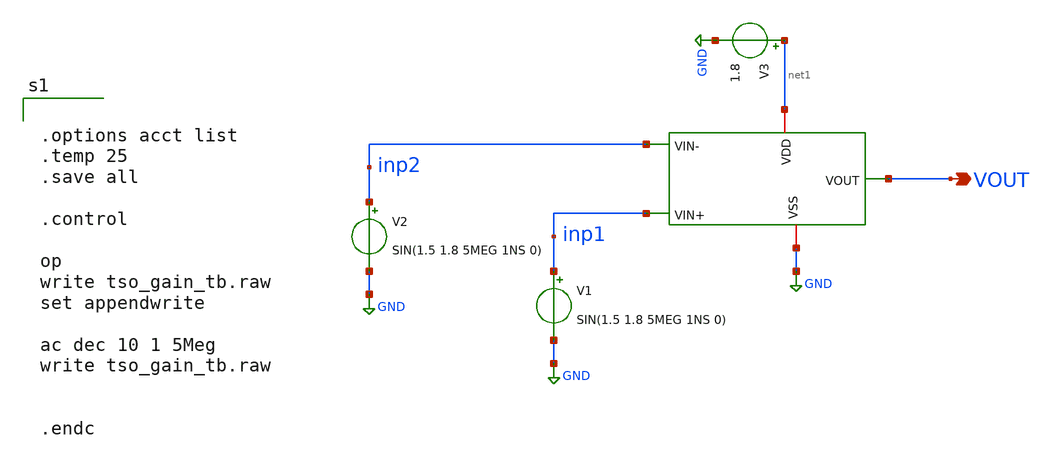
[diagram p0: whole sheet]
** sch_path: xschem/tso_gain_tb.sch
**.subckt tso_gain_tb VOUT
*.opin VOUT
x1 net1 VOUT inp2 inp1 GND tso
V1 inp1 GND SIN(1.5 1.8 5MEG 1NS 0)
V3 net1 GND 1.8
V2 inp2 GND SIN(1.5 1.8 5MEG 1NS 0)
**** begin user architecture code


.options acct list
.temp 25
.save all

.control

op
write tso_gain_tb.raw
set appendwrite

ac dec 10 1 5Meg
write tso_gain_tb.raw


.endc




** opencircuitdesign pdks install
.lib $::SKYWATER_MODELS/sky130.lib.spice tt


**** end user architecture code
**.ends

* expanding   symbol:  tso.sym # of pins=5
** sym_path: xschem/tso.sym
** sch_path: xschem/tso.sch
.subckt tso VDD VOUT VIN- VIN+ VSS
*.ipin VIN+
*.opin VOUT
*.iopin VSS
*.iopin VDD
*.ipin VIN-
XM1 net1 VIN- vs1 GND sky130_fd_pr__nfet_01v8 L=0.5 W=2.25 nf=1 ad='int((nf+1)/2) * W/nf * 0.29' as='int((nf+2)/2) * W/nf * 0.29'
+ pd='2*int((nf+1)/2) * (W/nf + 0.29)' ps='2*int((nf+2)/2) * (W/nf + 0.29)' nrd='0.29 / W' nrs='0.29 / W'
+ sa=0 sb=0 sd=0 mult=1 m=1
XM2 vd2 VIN+ vs1 GND sky130_fd_pr__nfet_01v8 L=0.5 W=2.25 nf=1 ad='int((nf+1)/2) * W/nf * 0.29' as='int((nf+2)/2) * W/nf * 0.29'
+ pd='2*int((nf+1)/2) * (W/nf + 0.29)' ps='2*int((nf+2)/2) * (W/nf + 0.29)' nrd='0.29 / W' nrs='0.29 / W'
+ sa=0 sb=0 sd=0 mult=1 m=1
XM3 vd1 vd1 VDD VDD sky130_fd_pr__pfet_01v8 L=0.5 W=15 nf=1 ad='int((nf+1)/2) * W/nf * 0.29' as='int((nf+2)/2) * W/nf * 0.29'
+ pd='2*int((nf+1)/2) * (W/nf + 0.29)' ps='2*int((nf+2)/2) * (W/nf + 0.29)' nrd='0.29 / W' nrs='0.29 / W'
+ sa=0 sb=0 sd=0 mult=1 m=1
XM4 vd2 vd1 VDD VDD sky130_fd_pr__pfet_01v8 L=0.5 W=15 nf=1 ad='int((nf+1)/2) * W/nf * 0.29' as='int((nf+2)/2) * W/nf * 0.29'
+ pd='2*int((nf+1)/2) * (W/nf + 0.29)' ps='2*int((nf+2)/2) * (W/nf + 0.29)' nrd='0.29 / W' nrs='0.29 / W'
+ sa=0 sb=0 sd=0 mult=1 m=1
XM5 net2 vgs5 VSS VSS sky130_fd_pr__nfet_01v8 L=0.5 W=0.75 nf=1 ad='int((nf+1)/2) * W/nf * 0.29' as='int((nf+2)/2) * W/nf * 0.29'
+ pd='2*int((nf+1)/2) * (W/nf + 0.29)' ps='2*int((nf+2)/2) * (W/nf + 0.29)' nrd='0.29 / W' nrs='0.29 / W'
+ sa=0 sb=0 sd=0 mult=1 m=1
XM6 VOUT vd2 VDD VDD sky130_fd_pr__pfet_01v8 L=0.5 W=73 nf=1 ad='int((nf+1)/2) * W/nf * 0.29' as='int((nf+2)/2) * W/nf * 0.29'
+ pd='2*int((nf+1)/2) * (W/nf + 0.29)' ps='2*int((nf+2)/2) * (W/nf + 0.29)' nrd='0.29 / W' nrs='0.29 / W'
+ sa=0 sb=0 sd=0 mult=1 m=1
XM7 VOUT vgs5 VSS VSS sky130_fd_pr__nfet_01v8 L=0.5 W=5.5 nf=1 ad='int((nf+1)/2) * W/nf * 0.29' as='int((nf+2)/2) * W/nf * 0.29'
+ pd='2*int((nf+1)/2) * (W/nf + 0.29)' ps='2*int((nf+2)/2) * (W/nf + 0.29)' nrd='0.29 / W' nrs='0.29 / W'
+ sa=0 sb=0 sd=0 mult=1 m=1
XM8 vgs5 vgs5 VSS VSS sky130_fd_pr__nfet_01v8 L=0.5 W=0.75 nf=1 ad='int((nf+1)/2) * W/nf * 0.29' as='int((nf+2)/2) * W/nf * 0.29'
+ pd='2*int((nf+1)/2) * (W/nf + 0.29)' ps='2*int((nf+2)/2) * (W/nf + 0.29)' nrd='0.29 / W' nrs='0.29 / W'
+ sa=0 sb=0 sd=0 mult=1 m=1
XC1 VOUT vd2 sky130_fd_pr__cap_mim_m3_1 W=25 L=25 MF=4 m=4
XC2 VOUT VSS sky130_fd_pr__cap_mim_m3_1 W=25 L=25 MF=8 m=8
I0 VDD vgs5 0.025m
v5 vd1 net1 0
.save i(v5)
v1 vs1 net2 0
.save i(v1)
.ends

.GLOBAL GND
.end
